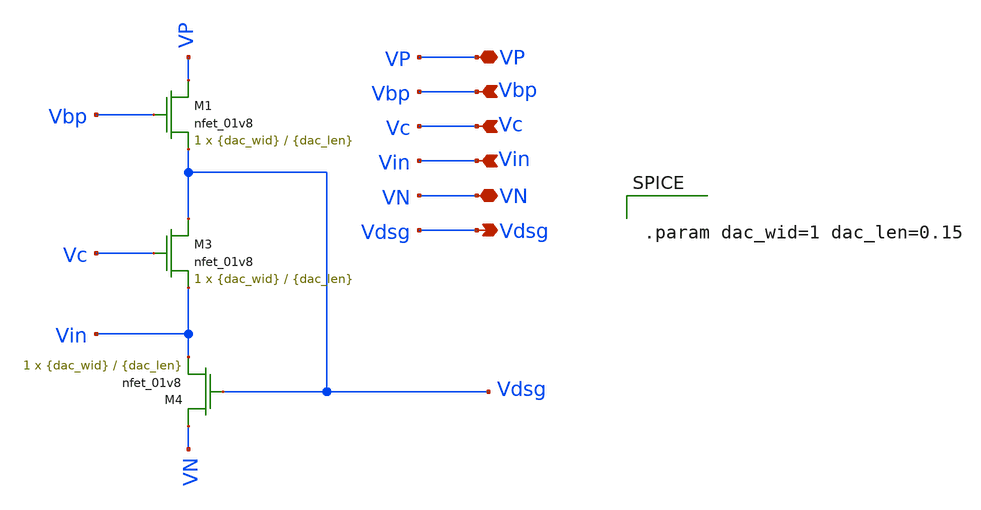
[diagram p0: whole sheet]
** sch_path: fvf.sch
**.subckt fvf VP Vbp Vc Vin VN Vdsg
*.iopin VP
*.ipin Vbp
*.ipin Vc
*.ipin Vin
*.iopin VN
*.opin Vdsg
XM1 VP Vbp Vdsg VN sky130_fd_pr__nfet_01v8 L={dac_len} W={dac_wid} nf=1 ad='int((nf+1)/2) * W/nf * 0.29'
+ as='int((nf+2)/2) * W/nf * 0.29' pd='2*int((nf+1)/2) * (W/nf + 0.29)' ps='2*int((nf+2)/2) * (W/nf + 0.29)'
+ nrd='0.29 / W' nrs='0.29 / W' sa=0 sb=0 sd=0 mult=1 m=1
XM3 Vdsg Vc Vin GND sky130_fd_pr__nfet_01v8 L={dac_len} W={dac_wid} nf=1 ad='int((nf+1)/2) * W/nf * 0.29'
+ as='int((nf+2)/2) * W/nf * 0.29' pd='2*int((nf+1)/2) * (W/nf + 0.29)' ps='2*int((nf+2)/2) * (W/nf + 0.29)'
+ nrd='0.29 / W' nrs='0.29 / W' sa=0 sb=0 sd=0 mult=1 m=1
XM4 VN Vdsg Vin VN sky130_fd_pr__nfet_01v8 L={dac_len} W={dac_wid} nf=1 ad='int((nf+1)/2) * W/nf * 0.29'
+ as='int((nf+2)/2) * W/nf * 0.29' pd='2*int((nf+1)/2) * (W/nf + 0.29)' ps='2*int((nf+2)/2) * (W/nf + 0.29)'
+ nrd='0.29 / W' nrs='0.29 / W' sa=0 sb=0 sd=0 mult=1 m=1
**** begin user architecture code


.param dac_wid=1 dac_len=0.15


**** end user architecture code
**.ends
.end
